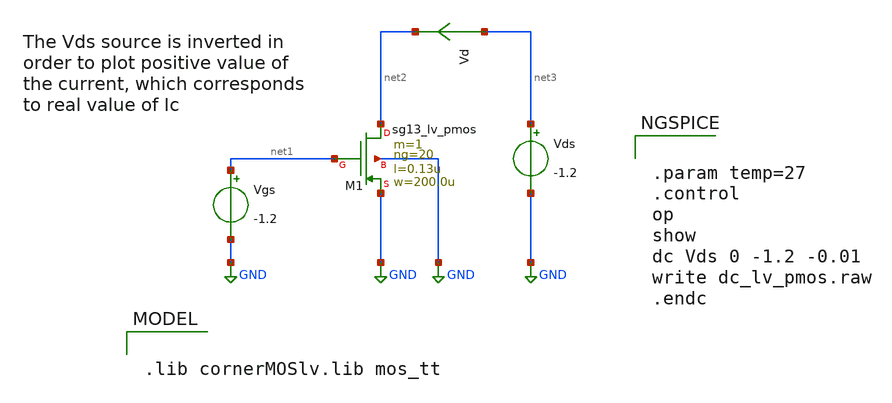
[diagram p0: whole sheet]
** sch_path: CHIPCHILE_CANELOS24_WorkshopTO/design_data/xschem/tgate/dc_lv_pmos.sch
* Copyright 2023 IHP PDK Authors
**.subckt dc_lv_pmos
Vgs net1 GND -1.2
Vds net3 GND -1.2
XM1 net2 net1 GND GND sg13_lv_pmos w=200.0u l=0.13u ng=20 m=1 mm_ok=1
Vd net3 net2 0
.save i(vd)
**** begin user architecture code

.lib cornerMOSlv.lib mos_tt



.param temp=27
.control
op
show
dc Vds 0 -1.2 -0.01
write dc_lv_pmos.raw
.endc


**** end user architecture code
**.ends
.GLOBAL GND
.end
